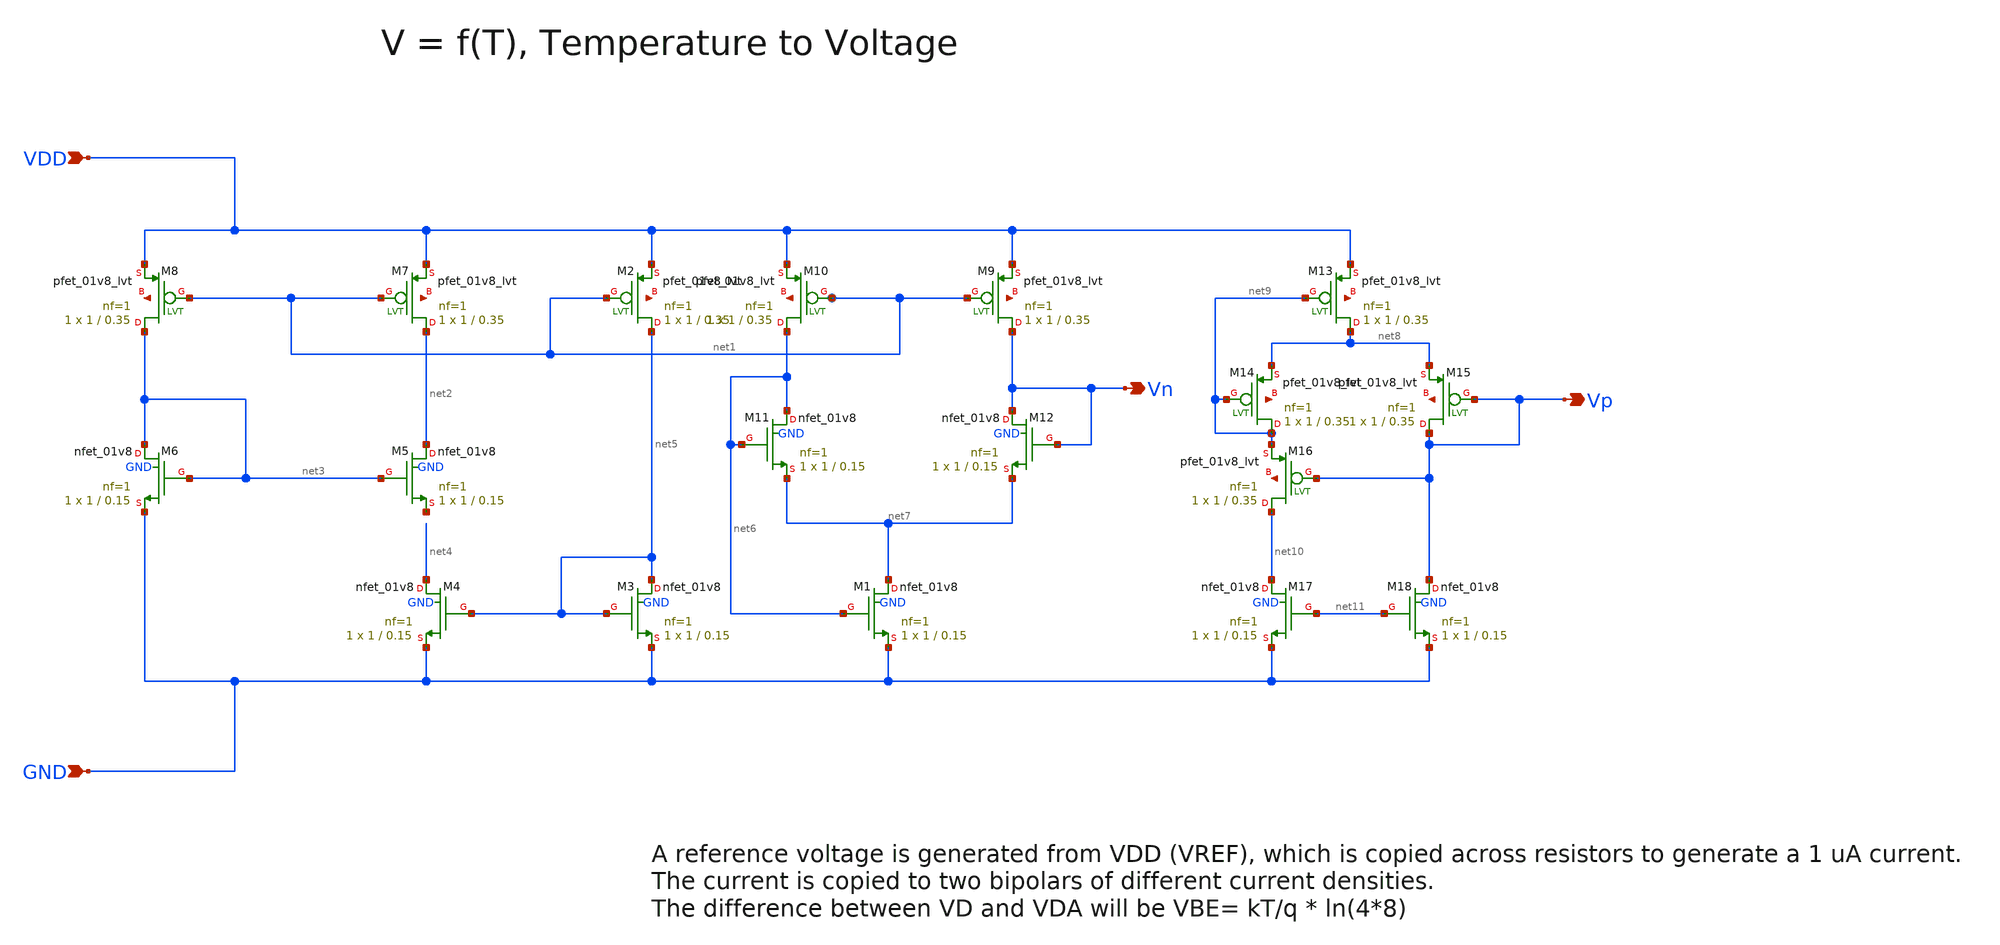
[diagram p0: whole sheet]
** sch_path: design/CNR_GR06_SKY130NM/CNR_GR06_test.sch
**.subckt CNR_GR06_test VDD GND Vn Vp
*.ipin VDD
*.ipin GND
*.opin Vn
*.opin Vp
XM1 net7 net6 GND GND sky130_fd_pr__nfet_01v8 L=0.15 W=1 nf=1 ad='int((nf+1)/2) * W/nf * 0.29' as='int((nf+2)/2) * W/nf * 0.29'
+ pd='2*int((nf+1)/2) * (W/nf + 0.29)' ps='2*int((nf+2)/2) * (W/nf + 0.29)' nrd='0.29 / W' nrs='0.29 / W'
+ sa=0 sb=0 sd=0 mult=1 m=1
XM2 net5 net1 VDD net12 sky130_fd_pr__pfet_01v8_lvt L=0.35 W=1 nf=1 ad='int((nf+1)/2) * W/nf * 0.29'
+ as='int((nf+2)/2) * W/nf * 0.29' pd='2*int((nf+1)/2) * (W/nf + 0.29)' ps='2*int((nf+2)/2) * (W/nf + 0.29)'
+ nrd='0.29 / W' nrs='0.29 / W' sa=0 sb=0 sd=0 mult=1 m=1
XM3 net5 net5 GND GND sky130_fd_pr__nfet_01v8 L=0.15 W=1 nf=1 ad='int((nf+1)/2) * W/nf * 0.29' as='int((nf+2)/2) * W/nf * 0.29'
+ pd='2*int((nf+1)/2) * (W/nf + 0.29)' ps='2*int((nf+2)/2) * (W/nf + 0.29)' nrd='0.29 / W' nrs='0.29 / W'
+ sa=0 sb=0 sd=0 mult=1 m=1
XM4 net4 net5 GND GND sky130_fd_pr__nfet_01v8 L=0.15 W=1 nf=1 ad='int((nf+1)/2) * W/nf * 0.29' as='int((nf+2)/2) * W/nf * 0.29'
+ pd='2*int((nf+1)/2) * (W/nf + 0.29)' ps='2*int((nf+2)/2) * (W/nf + 0.29)' nrd='0.29 / W' nrs='0.29 / W'
+ sa=0 sb=0 sd=0 mult=1 m=1
XM5 net2 net3 net13 GND sky130_fd_pr__nfet_01v8 L=0.15 W=1 nf=1 ad='int((nf+1)/2) * W/nf * 0.29' as='int((nf+2)/2) * W/nf * 0.29'
+ pd='2*int((nf+1)/2) * (W/nf + 0.29)' ps='2*int((nf+2)/2) * (W/nf + 0.29)' nrd='0.29 / W' nrs='0.29 / W'
+ sa=0 sb=0 sd=0 mult=1 m=1
XM6 net3 net3 GND GND sky130_fd_pr__nfet_01v8 L=0.15 W=1 nf=1 ad='int((nf+1)/2) * W/nf * 0.29' as='int((nf+2)/2) * W/nf * 0.29'
+ pd='2*int((nf+1)/2) * (W/nf + 0.29)' ps='2*int((nf+2)/2) * (W/nf + 0.29)' nrd='0.29 / W' nrs='0.29 / W'
+ sa=0 sb=0 sd=0 mult=1 m=1
XM7 net2 net1 VDD net14 sky130_fd_pr__pfet_01v8_lvt L=0.35 W=1 nf=1 ad='int((nf+1)/2) * W/nf * 0.29'
+ as='int((nf+2)/2) * W/nf * 0.29' pd='2*int((nf+1)/2) * (W/nf + 0.29)' ps='2*int((nf+2)/2) * (W/nf + 0.29)'
+ nrd='0.29 / W' nrs='0.29 / W' sa=0 sb=0 sd=0 mult=1 m=1
XM8 net3 net1 VDD net15 sky130_fd_pr__pfet_01v8_lvt L=0.35 W=1 nf=1 ad='int((nf+1)/2) * W/nf * 0.29'
+ as='int((nf+2)/2) * W/nf * 0.29' pd='2*int((nf+1)/2) * (W/nf + 0.29)' ps='2*int((nf+2)/2) * (W/nf + 0.29)'
+ nrd='0.29 / W' nrs='0.29 / W' sa=0 sb=0 sd=0 mult=1 m=1
XM9 Vn net1 VDD net16 sky130_fd_pr__pfet_01v8_lvt L=0.35 W=1 nf=1 ad='int((nf+1)/2) * W/nf * 0.29' as='int((nf+2)/2) * W/nf * 0.29'
+ pd='2*int((nf+1)/2) * (W/nf + 0.29)' ps='2*int((nf+2)/2) * (W/nf + 0.29)' nrd='0.29 / W' nrs='0.29 / W'
+ sa=0 sb=0 sd=0 mult=1 m=1
XM10 net6 net1 VDD net17 sky130_fd_pr__pfet_01v8_lvt L=0.35 W=1 nf=1 ad='int((nf+1)/2) * W/nf * 0.29'
+ as='int((nf+2)/2) * W/nf * 0.29' pd='2*int((nf+1)/2) * (W/nf + 0.29)' ps='2*int((nf+2)/2) * (W/nf + 0.29)'
+ nrd='0.29 / W' nrs='0.29 / W' sa=0 sb=0 sd=0 mult=1 m=1
XM11 net6 net6 net7 GND sky130_fd_pr__nfet_01v8 L=0.15 W=1 nf=1 ad='int((nf+1)/2) * W/nf * 0.29' as='int((nf+2)/2) * W/nf * 0.29'
+ pd='2*int((nf+1)/2) * (W/nf + 0.29)' ps='2*int((nf+2)/2) * (W/nf + 0.29)' nrd='0.29 / W' nrs='0.29 / W'
+ sa=0 sb=0 sd=0 mult=1 m=1
XM12 Vn Vn net7 GND sky130_fd_pr__nfet_01v8 L=0.15 W=1 nf=1 ad='int((nf+1)/2) * W/nf * 0.29' as='int((nf+2)/2) * W/nf * 0.29'
+ pd='2*int((nf+1)/2) * (W/nf + 0.29)' ps='2*int((nf+2)/2) * (W/nf + 0.29)' nrd='0.29 / W' nrs='0.29 / W'
+ sa=0 sb=0 sd=0 mult=1 m=1
XM13 net8 net9 VDD net18 sky130_fd_pr__pfet_01v8_lvt L=0.35 W=1 nf=1 ad='int((nf+1)/2) * W/nf * 0.29'
+ as='int((nf+2)/2) * W/nf * 0.29' pd='2*int((nf+1)/2) * (W/nf + 0.29)' ps='2*int((nf+2)/2) * (W/nf + 0.29)'
+ nrd='0.29 / W' nrs='0.29 / W' sa=0 sb=0 sd=0 mult=1 m=1
XM17 net10 net11 GND GND sky130_fd_pr__nfet_01v8 L=0.15 W=1 nf=1 ad='int((nf+1)/2) * W/nf * 0.29' as='int((nf+2)/2) * W/nf * 0.29'
+ pd='2*int((nf+1)/2) * (W/nf + 0.29)' ps='2*int((nf+2)/2) * (W/nf + 0.29)' nrd='0.29 / W' nrs='0.29 / W'
+ sa=0 sb=0 sd=0 mult=1 m=1
XM18 Vp net11 GND GND sky130_fd_pr__nfet_01v8 L=0.15 W=1 nf=1 ad='int((nf+1)/2) * W/nf * 0.29' as='int((nf+2)/2) * W/nf * 0.29'
+ pd='2*int((nf+1)/2) * (W/nf + 0.29)' ps='2*int((nf+2)/2) * (W/nf + 0.29)' nrd='0.29 / W' nrs='0.29 / W'
+ sa=0 sb=0 sd=0 mult=1 m=1
XM14 net9 net9 net8 net19 sky130_fd_pr__pfet_01v8_lvt L=0.35 W=1 nf=1 ad='int((nf+1)/2) * W/nf * 0.29'
+ as='int((nf+2)/2) * W/nf * 0.29' pd='2*int((nf+1)/2) * (W/nf + 0.29)' ps='2*int((nf+2)/2) * (W/nf + 0.29)'
+ nrd='0.29 / W' nrs='0.29 / W' sa=0 sb=0 sd=0 mult=1 m=1
XM15 Vp Vp net8 net20 sky130_fd_pr__pfet_01v8_lvt L=0.35 W=1 nf=1 ad='int((nf+1)/2) * W/nf * 0.29' as='int((nf+2)/2) * W/nf * 0.29'
+ pd='2*int((nf+1)/2) * (W/nf + 0.29)' ps='2*int((nf+2)/2) * (W/nf + 0.29)' nrd='0.29 / W' nrs='0.29 / W'
+ sa=0 sb=0 sd=0 mult=1 m=1
XM16 net10 Vp net9 net21 sky130_fd_pr__pfet_01v8_lvt L=0.35 W=1 nf=1 ad='int((nf+1)/2) * W/nf * 0.29'
+ as='int((nf+2)/2) * W/nf * 0.29' pd='2*int((nf+1)/2) * (W/nf + 0.29)' ps='2*int((nf+2)/2) * (W/nf + 0.29)'
+ nrd='0.29 / W' nrs='0.29 / W' sa=0 sb=0 sd=0 mult=1 m=1
**.ends
.end
